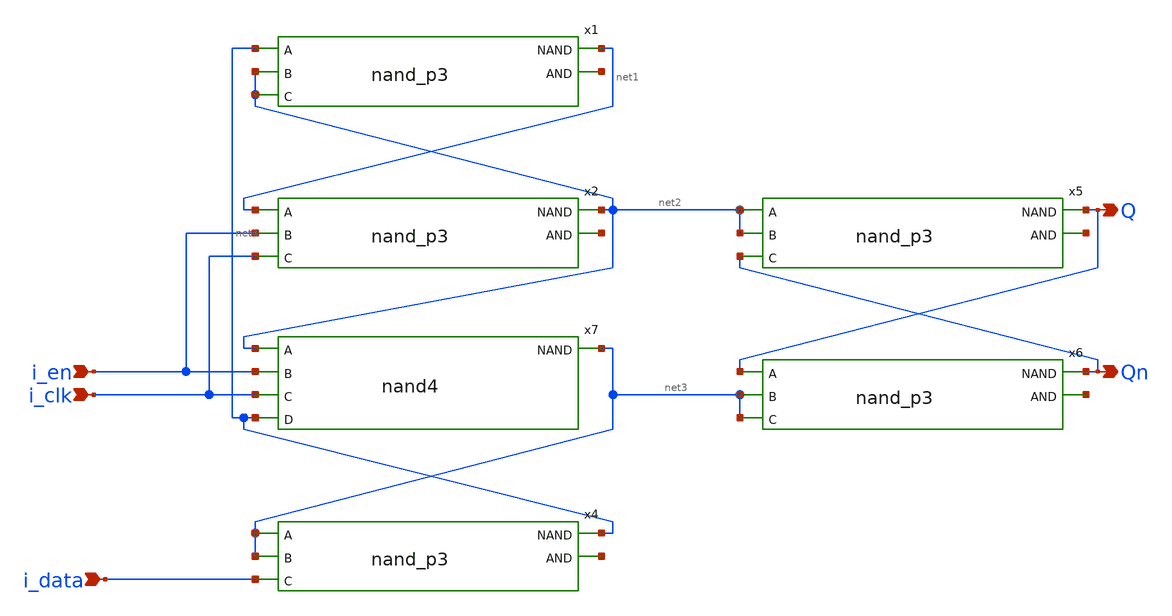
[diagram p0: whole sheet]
** sch_path: elements/edff.sch
**.subckt edff i_clk i_data Q Qn i_en
*.ipin i_clk
*.ipin i_data
*.opin Q
*.opin Qn
*.ipin i_en
x1 net1 net5 net4 net2 net2 nand_p3
x2 net2 net6 net1 i_en i_clk nand_p3
x4 net4 net7 net3 net3 i_data nand_p3
x5 Q net8 net2 net2 Qn nand_p3
x6 Qn net9 Q net3 net3 nand_p3
x7 net3 net2 i_en i_clk net4 nand4
**.ends

* expanding   symbol:  /mnt/d/Projects/RISC-V/core_tiny/asic/elements/nand_p3.sym # of pins=5
** sym_path: elements/nand_p3.sym
** sch_path: elements/nand_p3.sch
.subckt nand_p3 NAND AND A B C
*.ipin A
*.opin NAND
*.opin AND
*.ipin B
*.ipin C
XM1 NAND A VCC VCC sky130_fd_pr__pfet_01v8 L=0.15 W=1 nf=1 ad='int((nf+1)/2) * W/nf * 0.29' as='int((nf+2)/2) * W/nf * 0.29'
+ pd='2*int((nf+1)/2) * (W/nf + 0.29)' ps='2*int((nf+2)/2) * (W/nf + 0.29)' nrd='0.29 / W' nrs='0.29 / W'
+ sa=0 sb=0 sd=0 mult=1 m=1
XM2 NAND B VCC VCC sky130_fd_pr__pfet_01v8 L=0.15 W=1 nf=1 ad='int((nf+1)/2) * W/nf * 0.29' as='int((nf+2)/2) * W/nf * 0.29'
+ pd='2*int((nf+1)/2) * (W/nf + 0.29)' ps='2*int((nf+2)/2) * (W/nf + 0.29)' nrd='0.29 / W' nrs='0.29 / W'
+ sa=0 sb=0 sd=0 mult=1 m=1
.save v(vcc)
XM3 NAND C VCC VCC sky130_fd_pr__pfet_01v8 L=0.15 W=1 nf=1 ad='int((nf+1)/2) * W/nf * 0.29' as='int((nf+2)/2) * W/nf * 0.29'
+ pd='2*int((nf+1)/2) * (W/nf + 0.29)' ps='2*int((nf+2)/2) * (W/nf + 0.29)' nrd='0.29 / W' nrs='0.29 / W'
+ sa=0 sb=0 sd=0 mult=1 m=1
XM6 NAND A net1 VSS sky130_fd_pr__nfet_01v8 L=0.15 W=0.65 nf=1 ad='int((1 + 1)/2) * 0.65 / 1 * 0.29'
+ as='int((1 + 2)/2) * 0.65 / 1 * 0.29' pd='2*int((1 + 1)/2) * (0.65 / 1 + 0.29)' ps='2*int((1 + 2)/2) * (0.65 / 1 + 0.29)'
+ nrd='0.29 / 0.65 ' nrs='0.29 / 0.65 ' sa=0 sb=0 sd=0 mult=1 m=1
XM7 net1 B net2 VSS sky130_fd_pr__nfet_01v8 L=0.15 W=0.65 nf=1 ad='int((1 + 1)/2) * 0.65 / 1 * 0.29'
+ as='int((1 + 2)/2) * 0.65 / 1 * 0.29' pd='2*int((1 + 1)/2) * (0.65 / 1 + 0.29)' ps='2*int((1 + 2)/2) * (0.65 / 1 + 0.29)'
+ nrd='0.29 / 0.65 ' nrs='0.29 / 0.65 ' sa=0 sb=0 sd=0 mult=1 m=1
XM8 net2 C VSS VSS sky130_fd_pr__nfet_01v8 L=0.15 W=0.65 nf=1 ad='int((1 + 1)/2) * 0.65 / 1 * 0.29' as='int((1 + 2)/2) * 0.65 / 1 * 0.29'
+ pd='2*int((1 + 1)/2) * (0.65 / 1 + 0.29)' ps='2*int((1 + 2)/2) * (0.65 / 1 + 0.29)' nrd='0.29 / 0.65 '
+ nrs='0.29 / 0.65 ' sa=0 sb=0 sd=0 mult=1 m=1
XM4 AND NAND VCC VCC sky130_fd_pr__pfet_01v8 L=0.15 W=1 nf=1 ad='int((nf+1)/2) * W/nf * 0.29' as='int((nf+2)/2) * W/nf * 0.29'
+ pd='2*int((nf+1)/2) * (W/nf + 0.29)' ps='2*int((nf+2)/2) * (W/nf + 0.29)' nrd='0.29 / W' nrs='0.29 / W'
+ sa=0 sb=0 sd=0 mult=1 m=1
XM5 AND NAND VSS VSS sky130_fd_pr__nfet_01v8 L=0.15 W=0.65 nf=1 ad='int((1 + 1)/2) * 0.65 / 1 * 0.29'
+ as='int((1 + 2)/2) * 0.65 / 1 * 0.29' pd='2*int((1 + 1)/2) * (0.65 / 1 + 0.29)' ps='2*int((1 + 2)/2) * (0.65 / 1 + 0.29)'
+ nrd='0.29 / 0.65 ' nrs='0.29 / 0.65 ' sa=0 sb=0 sd=0 mult=1 m=1
.ends


* expanding   symbol:  /mnt/d/Projects/RISC-V/core_tiny/asic/elements/nand4.sym # of pins=5
** sym_path: elements/nand4.sym
** sch_path: elements/nand4.sch
.subckt nand4 NAND A B C D
*.ipin A
*.opin NAND
*.ipin B
*.ipin C
*.ipin D
XM1 NAND A VCC VCC sky130_fd_pr__pfet_01v8 L=0.15 W=1 nf=1 ad='int((nf+1)/2) * W/nf * 0.29' as='int((nf+2)/2) * W/nf * 0.29'
+ pd='2*int((nf+1)/2) * (W/nf + 0.29)' ps='2*int((nf+2)/2) * (W/nf + 0.29)' nrd='0.29 / W' nrs='0.29 / W'
+ sa=0 sb=0 sd=0 mult=1 m=1
XM2 NAND B VCC VCC sky130_fd_pr__pfet_01v8 L=0.15 W=1 nf=1 ad='int((nf+1)/2) * W/nf * 0.29' as='int((nf+2)/2) * W/nf * 0.29'
+ pd='2*int((nf+1)/2) * (W/nf + 0.29)' ps='2*int((nf+2)/2) * (W/nf + 0.29)' nrd='0.29 / W' nrs='0.29 / W'
+ sa=0 sb=0 sd=0 mult=1 m=1
XM3 NAND C VCC VCC sky130_fd_pr__pfet_01v8 L=0.15 W=1 nf=1 ad='int((nf+1)/2) * W/nf * 0.29' as='int((nf+2)/2) * W/nf * 0.29'
+ pd='2*int((nf+1)/2) * (W/nf + 0.29)' ps='2*int((nf+2)/2) * (W/nf + 0.29)' nrd='0.29 / W' nrs='0.29 / W'
+ sa=0 sb=0 sd=0 mult=1 m=1
XM6 NAND A net1 VSS sky130_fd_pr__nfet_01v8 L=0.15 W=0.65 nf=1 ad='int((1 + 1)/2) * 0.65 / 1 * 0.29'
+ as='int((1 + 2)/2) * 0.65 / 1 * 0.29' pd='2*int((1 + 1)/2) * (0.65 / 1 + 0.29)' ps='2*int((1 + 2)/2) * (0.65 / 1 + 0.29)'
+ nrd='0.29 / 0.65 ' nrs='0.29 / 0.65 ' sa=0 sb=0 sd=0 mult=1 m=1
XM7 net1 B net2 VSS sky130_fd_pr__nfet_01v8 L=0.15 W=0.65 nf=1 ad='int((1 + 1)/2) * 0.65 / 1 * 0.29'
+ as='int((1 + 2)/2) * 0.65 / 1 * 0.29' pd='2*int((1 + 1)/2) * (0.65 / 1 + 0.29)' ps='2*int((1 + 2)/2) * (0.65 / 1 + 0.29)'
+ nrd='0.29 / 0.65 ' nrs='0.29 / 0.65 ' sa=0 sb=0 sd=0 mult=1 m=1
XM8 net2 C net3 VSS sky130_fd_pr__nfet_01v8 L=0.15 W=0.65 nf=1 ad='int((1 + 1)/2) * 0.65 / 1 * 0.29'
+ as='int((1 + 2)/2) * 0.65 / 1 * 0.29' pd='2*int((1 + 1)/2) * (0.65 / 1 + 0.29)' ps='2*int((1 + 2)/2) * (0.65 / 1 + 0.29)'
+ nrd='0.29 / 0.65 ' nrs='0.29 / 0.65 ' sa=0 sb=0 sd=0 mult=1 m=1
XM4 NAND D VCC VCC sky130_fd_pr__pfet_01v8 L=0.15 W=1 nf=1 ad='int((nf+1)/2) * W/nf * 0.29' as='int((nf+2)/2) * W/nf * 0.29'
+ pd='2*int((nf+1)/2) * (W/nf + 0.29)' ps='2*int((nf+2)/2) * (W/nf + 0.29)' nrd='0.29 / W' nrs='0.29 / W'
+ sa=0 sb=0 sd=0 mult=1 m=1
XM5 net3 D VSS VSS sky130_fd_pr__nfet_01v8 L=0.15 W=0.65 nf=1 ad='int((1 + 1)/2) * 0.65 / 1 * 0.29' as='int((1 + 2)/2) * 0.65 / 1 * 0.29'
+ pd='2*int((1 + 1)/2) * (0.65 / 1 + 0.29)' ps='2*int((1 + 2)/2) * (0.65 / 1 + 0.29)' nrd='0.29 / 0.65 '
+ nrs='0.29 / 0.65 ' sa=0 sb=0 sd=0 mult=1 m=1
.ends

.GLOBAL VCC
.GLOBAL VSS
.end
